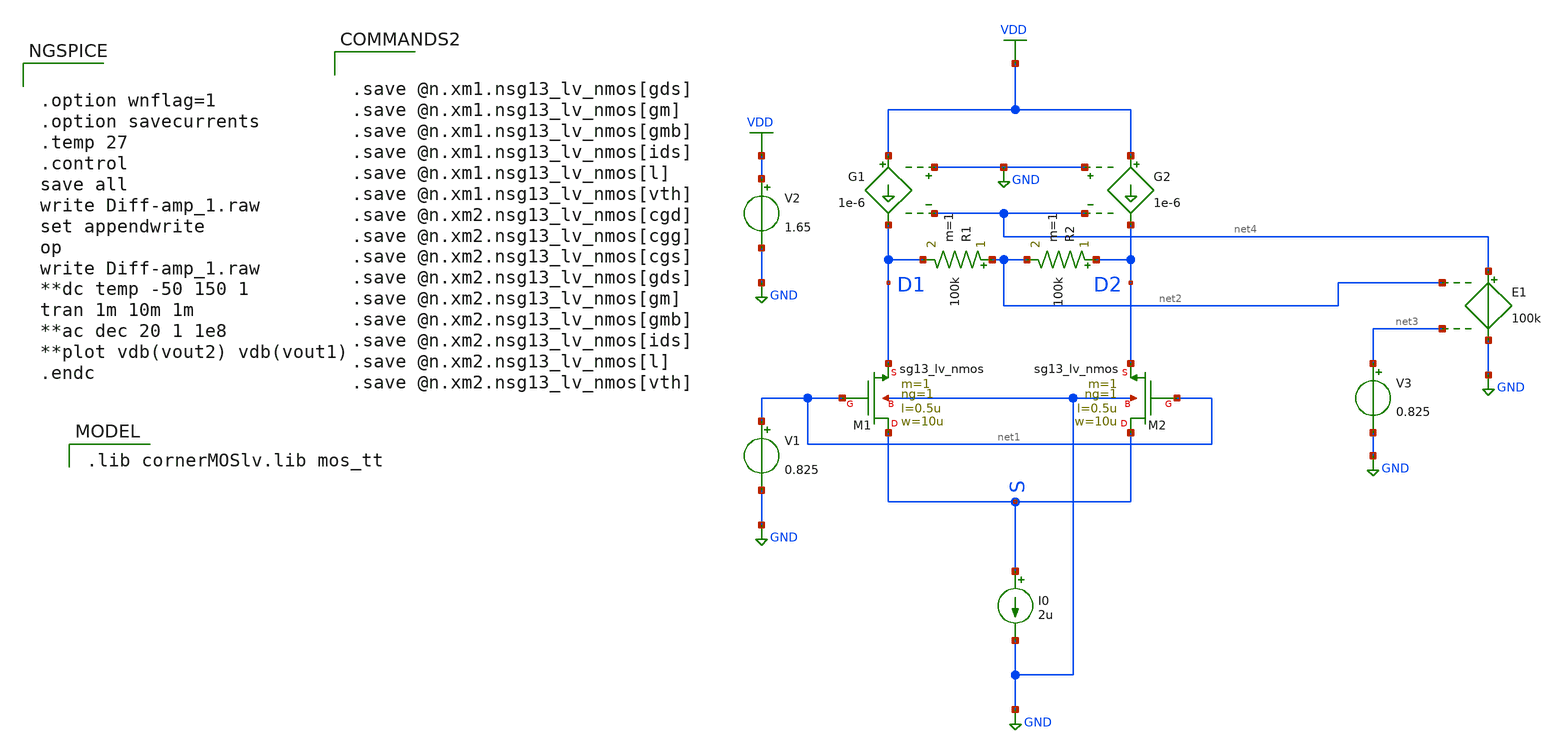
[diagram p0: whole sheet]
** sch_path: VLSI25/submitted_notebooks/Wrøngm/Schematics/Diff-amp_1.sch
**.subckt Diff-amp_1
XM1 S net1 D1 GND sg13_lv_nmos w=10u l=0.5u ng=1 m=1 mm_ok=1
XM2 S net1 D2 GND sg13_lv_nmos w=10u l=0.5u ng=1 m=1 mm_ok=1
I0 S GND 2u
V1 net1 GND 0.825
V2 VDD GND 1.65
E1 net4 GND net2 net3 100k
R1 net2 D1 100k m=1
R2 D2 net2 100k m=1
V3 net3 GND 0.825
G1 VDD D1 GND net4 1e-6
G2 VDD D2 GND net4 1e-6
**** begin user architecture code


.save @n.xm1.nsg13_lv_nmos[gds]
.save @n.xm1.nsg13_lv_nmos[gm]
.save @n.xm1.nsg13_lv_nmos[gmb]
.save @n.xm1.nsg13_lv_nmos[ids]
.save @n.xm1.nsg13_lv_nmos[l]
.save @n.xm1.nsg13_lv_nmos[vth]
.save @n.xm2.nsg13_lv_nmos[cgd]
.save @n.xm2.nsg13_lv_nmos[cgg]
.save @n.xm2.nsg13_lv_nmos[cgs]
.save @n.xm2.nsg13_lv_nmos[gds]
.save @n.xm2.nsg13_lv_nmos[gm]
.save @n.xm2.nsg13_lv_nmos[gmb]
.save @n.xm2.nsg13_lv_nmos[ids]
.save @n.xm2.nsg13_lv_nmos[l]
.save @n.xm2.nsg13_lv_nmos[vth]




.option wnflag=1
.option savecurrents
.temp 27
.control
save all
write Diff-amp_1.raw
set appendwrite
op
write Diff-amp_1.raw
**dc temp -50 150 1
tran 1m 10m 1m
**ac dec 20 1 1e8
**plot vdb(vout2) vdb(vout1)
.endc


 .lib cornerMOSlv.lib mos_tt

**** end user architecture code
**.ends
.GLOBAL GND
.GLOBAL VDD
.end
